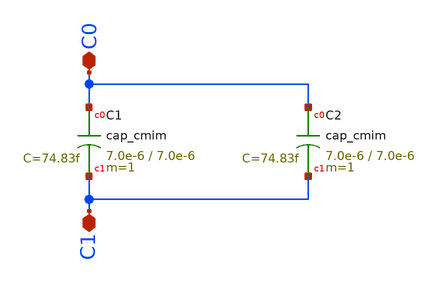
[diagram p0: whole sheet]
** sch_path: multiplier_support/schematic/sg13_cmim_2x.sch
**.subckt sg13_cmim_2x C0 C1
*.iopin C0
*.iopin C1
XC1 C0 C1 cap_cmim w=7.0e-6 l=7.0e-6 m=1 mm_ok=1
XC2 C0 C1 cap_cmim w=7.0e-6 l=7.0e-6 m=1 mm_ok=1
**.ends
.end
